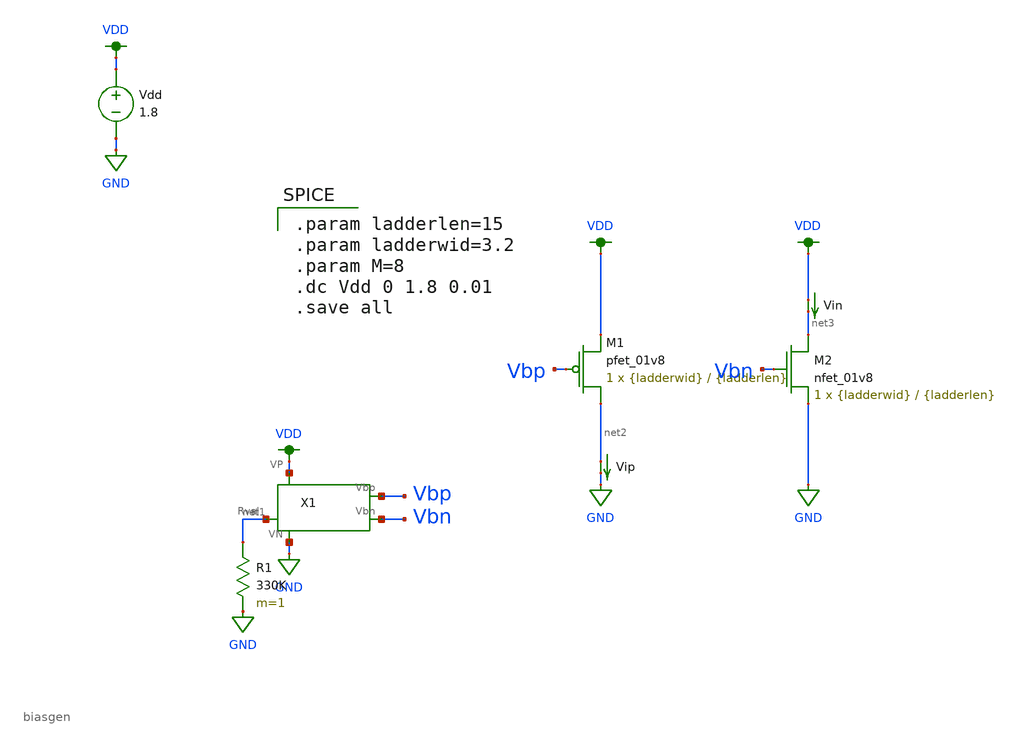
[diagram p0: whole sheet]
** sch_path: prelim-files/vbcalc.sch
**.subckt vbcalc
X1 net1 GND VDD Vbp Vbn biasgen
R1 net1 GND 330K m=1
XM1 net2 Vbp VDD VDD sky130_fd_pr__pfet_01v8 L={ladderlen} W={ladderwid} nf=1 ad='int((nf+1)/2) * W/nf * 0.29'
+ as='int((nf+2)/2) * W/nf * 0.29' pd='2*int((nf+1)/2) * (W/nf + 0.29)' ps='2*int((nf+2)/2) * (W/nf + 0.29)'
+ nrd='0.29 / W' nrs='0.29 / W' sa=0 sb=0 sd=0 mult=1 m=1
XM2 net3 Vbn GND GND sky130_fd_pr__nfet_01v8 L={ladderlen} W={ladderwid} nf=1 ad='int((nf+1)/2) * W/nf * 0.29'
+ as='int((nf+2)/2) * W/nf * 0.29' pd='2*int((nf+1)/2) * (W/nf + 0.29)' ps='2*int((nf+2)/2) * (W/nf + 0.29)'
+ nrd='0.29 / W' nrs='0.29 / W' sa=0 sb=0 sd=0 mult=1 m=1
Vip net2 GND 0
.save i(vip)
Vin VDD net3 0
.save i(vin)
Vdd VDD GND 1.8
**** begin user architecture code

.option wnflag=1
.param MC_SWITCH=0.0
.lib ~/skywater/skywater-pdk/libraries/sky130_fd_pr_ngspice/latest/models/sky130.lib.spice tt


.param ladderlen=15
.param ladderwid=3.2
.param M=8
.dc Vdd 0 1.8 0.01
.save all

**** end user architecture code
**.ends

* expanding   symbol:  /home/jonah/VLSI/MP4/biasgen.sym # of pins=5
** sym_path: prelim-files/biasgen.sym
** sch_path: prelim-files/biasgen.sch
.subckt biasgen Rval VN VP Vbp Vbn
*.iopin Rval
*.iopin VN
*.iopin VP
*.iopin Vbp
*.iopin Vbn
XM1 net1 net2 VN GND sky130_fd_pr__nfet_01v8 L={isourcelen} W={isourcewid} nf=1 ad='int((nf+1)/2) * W/nf * 0.29'
+ as='int((nf+2)/2) * W/nf * 0.29' pd='2*int((nf+1)/2) * (W/nf + 0.29)' ps='2*int((nf+2)/2) * (W/nf + 0.29)'
+ nrd='0.29 / W' nrs='0.29 / W' sa=0 sb=0 sd=0 mult=1 m=1
XM5 Rval net2 net2 GND sky130_fd_pr__nfet_01v8 L={isourcelen} W={isourcewid} nf=1 ad='int((nf+1)/2) * W/nf * 0.29'
+ as='int((nf+2)/2) * W/nf * 0.29' pd='2*int((nf+1)/2) * (W/nf + 0.29)' ps='2*int((nf+2)/2) * (W/nf + 0.29)'
+ nrd='0.29 / W' nrs='0.29 / W' sa=0 sb=0 sd=0 mult={M} m={M}
Viout net3 Vbn 0
.save i(viout)
XM8 VP Vbp net2 VDD sky130_fd_pr__pfet_01v8 L={isourcelen} W={isourcewid} nf=1 ad='int((nf+1)/2) * W/nf * 0.29'
+ as='int((nf+2)/2) * W/nf * 0.29' pd='2*int((nf+1)/2) * (W/nf + 0.29)' ps='2*int((nf+2)/2) * (W/nf + 0.29)'
+ nrd='0.29 / W' nrs='0.29 / W' sa=0 sb=0 sd=0 mult=1 m=1
XM3 VP net1 net1 VDD sky130_fd_pr__pfet_01v8 L={isourcelen} W={isourcewid} nf=1 ad='int((nf+1)/2) * W/nf * 0.29'
+ as='int((nf+2)/2) * W/nf * 0.29' pd='2*int((nf+1)/2) * (W/nf + 0.29)' ps='2*int((nf+2)/2) * (W/nf + 0.29)'
+ nrd='0.29 / W' nrs='0.29 / W' sa=0 sb=0 sd=0 mult=1 m=1
XM2 Vbp net1 VP VDD sky130_fd_pr__pfet_01v8 L={isourcelen} W={isourcewid} nf=1 ad='int((nf+1)/2) * W/nf * 0.29'
+ as='int((nf+2)/2) * W/nf * 0.29' pd='2*int((nf+1)/2) * (W/nf + 0.29)' ps='2*int((nf+2)/2) * (W/nf + 0.29)'
+ nrd='0.29 / W' nrs='0.29 / W' sa=0 sb=0 sd=0 mult=1 m=1
XM7 net3 Vbp VP VDD sky130_fd_pr__pfet_01v8 L={isourcelen} W={isourcewid} nf=1 ad='int((nf+1)/2) * W/nf * 0.29'
+ as='int((nf+2)/2) * W/nf * 0.29' pd='2*int((nf+1)/2) * (W/nf + 0.29)' ps='2*int((nf+2)/2) * (W/nf + 0.29)'
+ nrd='0.29 / W' nrs='0.29 / W' sa=0 sb=0 sd=0 mult=1 m=1
XM4 VN Vbn Vbp GND sky130_fd_pr__nfet_01v8 L={isourcelen} W={isourcewid} nf=1 ad='int((nf+1)/2) * W/nf * 0.29'
+ as='int((nf+2)/2) * W/nf * 0.29' pd='2*int((nf+1)/2) * (W/nf + 0.29)' ps='2*int((nf+2)/2) * (W/nf + 0.29)'
+ nrd='0.29 / W' nrs='0.29 / W' sa=0 sb=0 sd=0 mult=1 m=1
XM6 Vbn Vbn VN GND sky130_fd_pr__nfet_01v8 L={isourcelen} W={isourcewid} nf=1 ad='int((nf+1)/2) * W/nf * 0.29'
+ as='int((nf+2)/2) * W/nf * 0.29' pd='2*int((nf+1)/2) * (W/nf + 0.29)' ps='2*int((nf+2)/2) * (W/nf + 0.29)'
+ nrd='0.29 / W' nrs='0.29 / W' sa=0 sb=0 sd=0 mult=1 m=1
.ends

.GLOBAL GND
.GLOBAL VDD
.end
